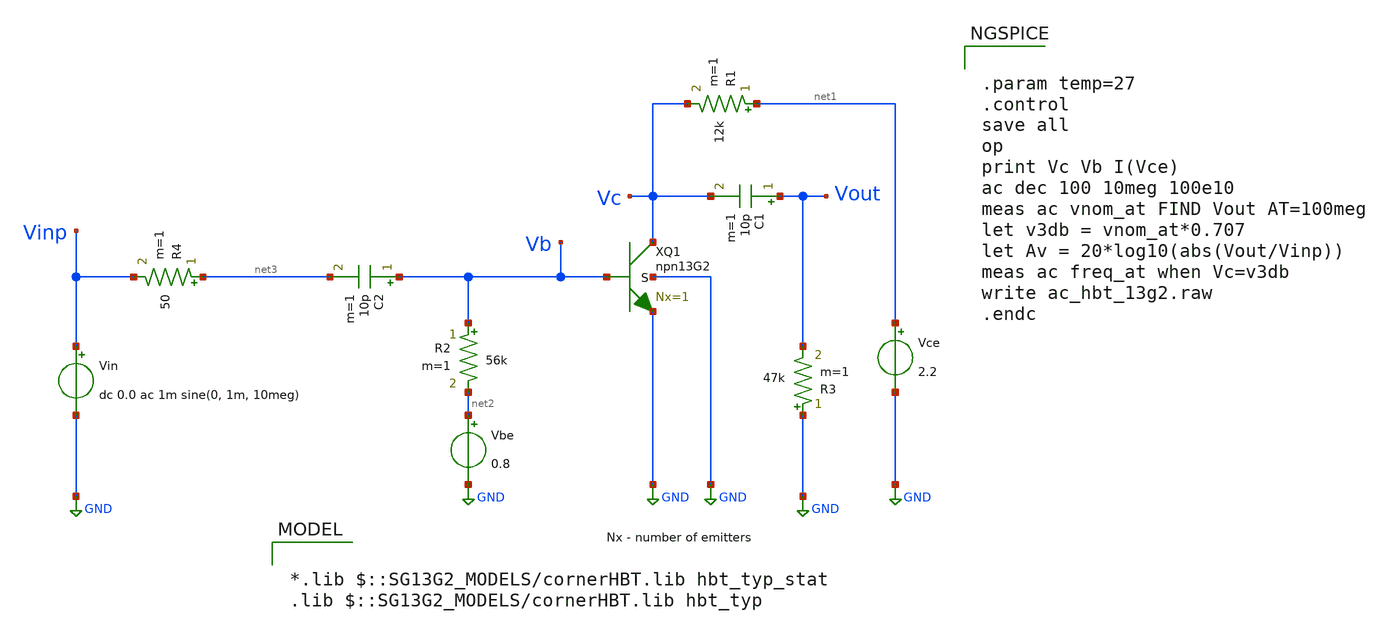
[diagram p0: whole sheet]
** sch_path: ihp-sg13g2/libs.tech/xschem/sg13g2_tests/ac_hbt_13g2.sch
* Copyright 2023 IHP PDK Authors
**.subckt ac_hbt_13g2
Vce net1 GND 2.2
XQ1 Vc Vb GND GND npn13G2 Nx=1
R1 net1 Vc 12k m=1
Vin Vinp GND dc 0.0 ac 1m sine(0, 1m, 10meg)
R2 Vb net2 56k m=1
Vbe net2 GND 0.8
R3 GND Vout 47k m=1
C1 Vout Vc 10p m=1
C2 Vb net3 10p m=1
R4 net3 Vinp 50 m=1
**** begin user architecture code

*.lib $::SG13G2_MODELS/cornerHBT.lib hbt_typ_stat
.lib $::SG13G2_MODELS/cornerHBT.lib hbt_typ



.param temp=27
.control
save all
op
print Vc Vb I(Vce)
ac dec 100 10meg 100e10
meas ac vnom_at FIND Vout AT=100meg
let v3db = vnom_at*0.707
let Av = 20*log10(abs(Vout/Vinp))
meas ac freq_at when Vc=v3db
write ac_hbt_13g2.raw
.endc


**** end user architecture code
**.ends
.GLOBAL GND
.end
